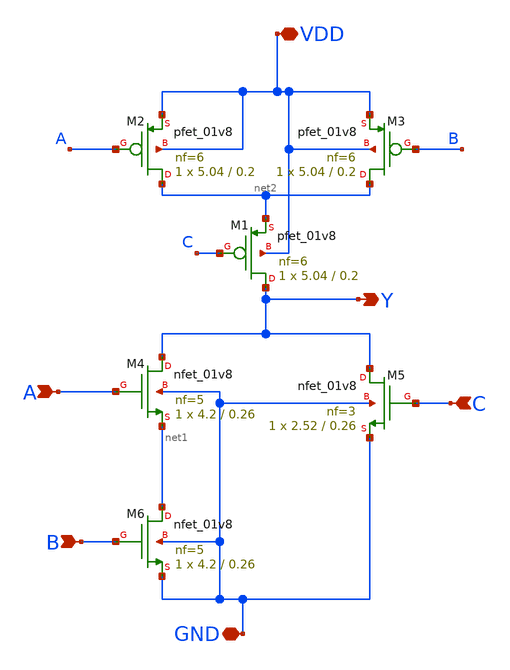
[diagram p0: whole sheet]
** sch_path: cells/AOI3X4/schematic/aoi3x4.sch
**.subckt aoi3x4 VDD GND A B C Y
*.iopin VDD
*.iopin GND
*.ipin A
*.ipin B
*.ipin C
*.opin Y
XM2 net2 A VDD VDD sky130_fd_pr__pfet_01v8 L=0.2 W=5.04 nf=6 ad='int((6 + 1)/2) * 5.04 / 6 * 0.29' as='int((6 + 2)/2) * 5.04 / 6 * 0.29'
+ pd='2*int((6 + 1)/2) * (5.04 / 6 + 0.29)' ps='2*int((6 + 2)/2) * (5.04 / 6 + 0.29)' nrd='0.29 / 5.04 '
+ nrs='0.29 / 5.04 ' sa=0 sb=0 sd=0 mult=1 m=1
XM3 net2 B VDD VDD sky130_fd_pr__pfet_01v8 L=0.2 W=5.04 nf=6 ad='int((6 + 1)/2) * 5.04 / 6 * 0.29' as='int((6 + 2)/2) * 5.04 / 6 * 0.29'
+ pd='2*int((6 + 1)/2) * (5.04 / 6 + 0.29)' ps='2*int((6 + 2)/2) * (5.04 / 6 + 0.29)' nrd='0.29 / 5.04 '
+ nrs='0.29 / 5.04 ' sa=0 sb=0 sd=0 mult=1 m=1
XM4 Y A net1 GND sky130_fd_pr__nfet_01v8 L=0.26 W=4.2 nf=5 ad='int((5 + 1)/2) * 4.2 / 5 * 0.29' as='int((5 + 2)/2) * 4.2 / 5 * 0.29'
+ pd='2*int((5 + 1)/2) * (4.2 / 5 + 0.29)' ps='2*int((5 + 2)/2) * (4.2 / 5 + 0.29)' nrd='0.29 / 4.2 ' nrs='0.29 / 4.2 '
+ sa=0 sb=0 sd=0 mult=1 m=1
XM5 Y C GND GND sky130_fd_pr__nfet_01v8 L=0.26 W=2.52 nf=3 ad='int((3 + 1)/2) * 2.52 / 3 * 0.29' as='int((3 + 2)/2) * 2.52 / 3 * 0.29'
+ pd='2*int((3 + 1)/2) * (2.52 / 3 + 0.29)' ps='2*int((3 + 2)/2) * (2.52 / 3 + 0.29)' nrd='0.29 / 2.52 '
+ nrs='0.29 / 2.52 ' sa=0 sb=0 sd=0 mult=1 m=1
XM1 Y C net2 VDD sky130_fd_pr__pfet_01v8 L=0.2 W=5.04 nf=6 ad='int((6 + 1)/2) * 5.04 / 6 * 0.29' as='int((6 + 2)/2) * 5.04 / 6 * 0.29'
+ pd='2*int((6 + 1)/2) * (5.04 / 6 + 0.29)' ps='2*int((6 + 2)/2) * (5.04 / 6 + 0.29)' nrd='0.29 / 5.04 '
+ nrs='0.29 / 5.04 ' sa=0 sb=0 sd=0 mult=1 m=1
XM6 net1 B GND GND sky130_fd_pr__nfet_01v8 L=0.26 W=4.2 nf=5 ad='int((5 + 1)/2) * 4.2 / 5 * 0.29' as='int((5 + 2)/2) * 4.2 / 5 * 0.29'
+ pd='2*int((5 + 1)/2) * (4.2 / 5 + 0.29)' ps='2*int((5 + 2)/2) * (4.2 / 5 + 0.29)' nrd='0.29 / 4.2 ' nrs='0.29 / 4.2 '
+ sa=0 sb=0 sd=0 mult=1 m=1
**.ends
.end
